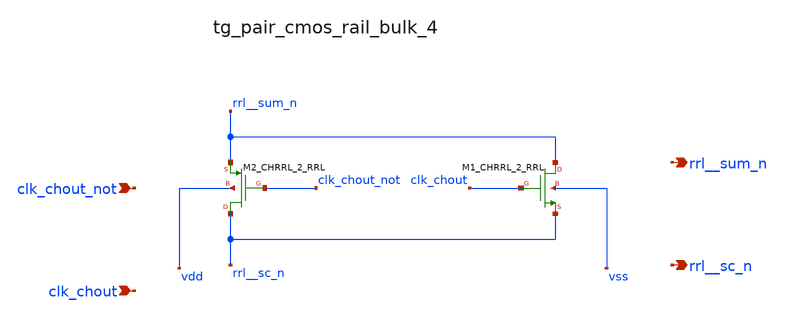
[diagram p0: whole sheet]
** sch_path: analog-db/raw/ia_004_fan_chopper_rrl/hier/blocks/tg_pair_cmos_rail_bulk_4.sch
**.subckt tg_pair_cmos_rail_bulk_4 clk_chout_not clk_chout rrl__sum_n rrl__sc_n
*.ipin clk_chout_not
*.ipin clk_chout
*.opin rrl__sum_n
*.opin rrl__sc_n
XM1_CHRRL_2_RRL rrl__sum_n clk_chout rrl__sc_n vss sg13_lv_nmos w=x_dut_xm1_chrrl_2_rrl_w
+ l=x_dut_xm1_chrrl_2_rrl_l ng=1 m=x_dut_xm1_chrrl_2_rrl_m
XM2_CHRRL_2_RRL rrl__sc_n clk_chout_not rrl__sum_n vdd sg13_lv_pmos w=x_dut_xm2_chrrl_2_rrl_w
+ l=x_dut_xm2_chrrl_2_rrl_l ng=1 m=x_dut_xm2_chrrl_2_rrl_m
**.ends
.end
